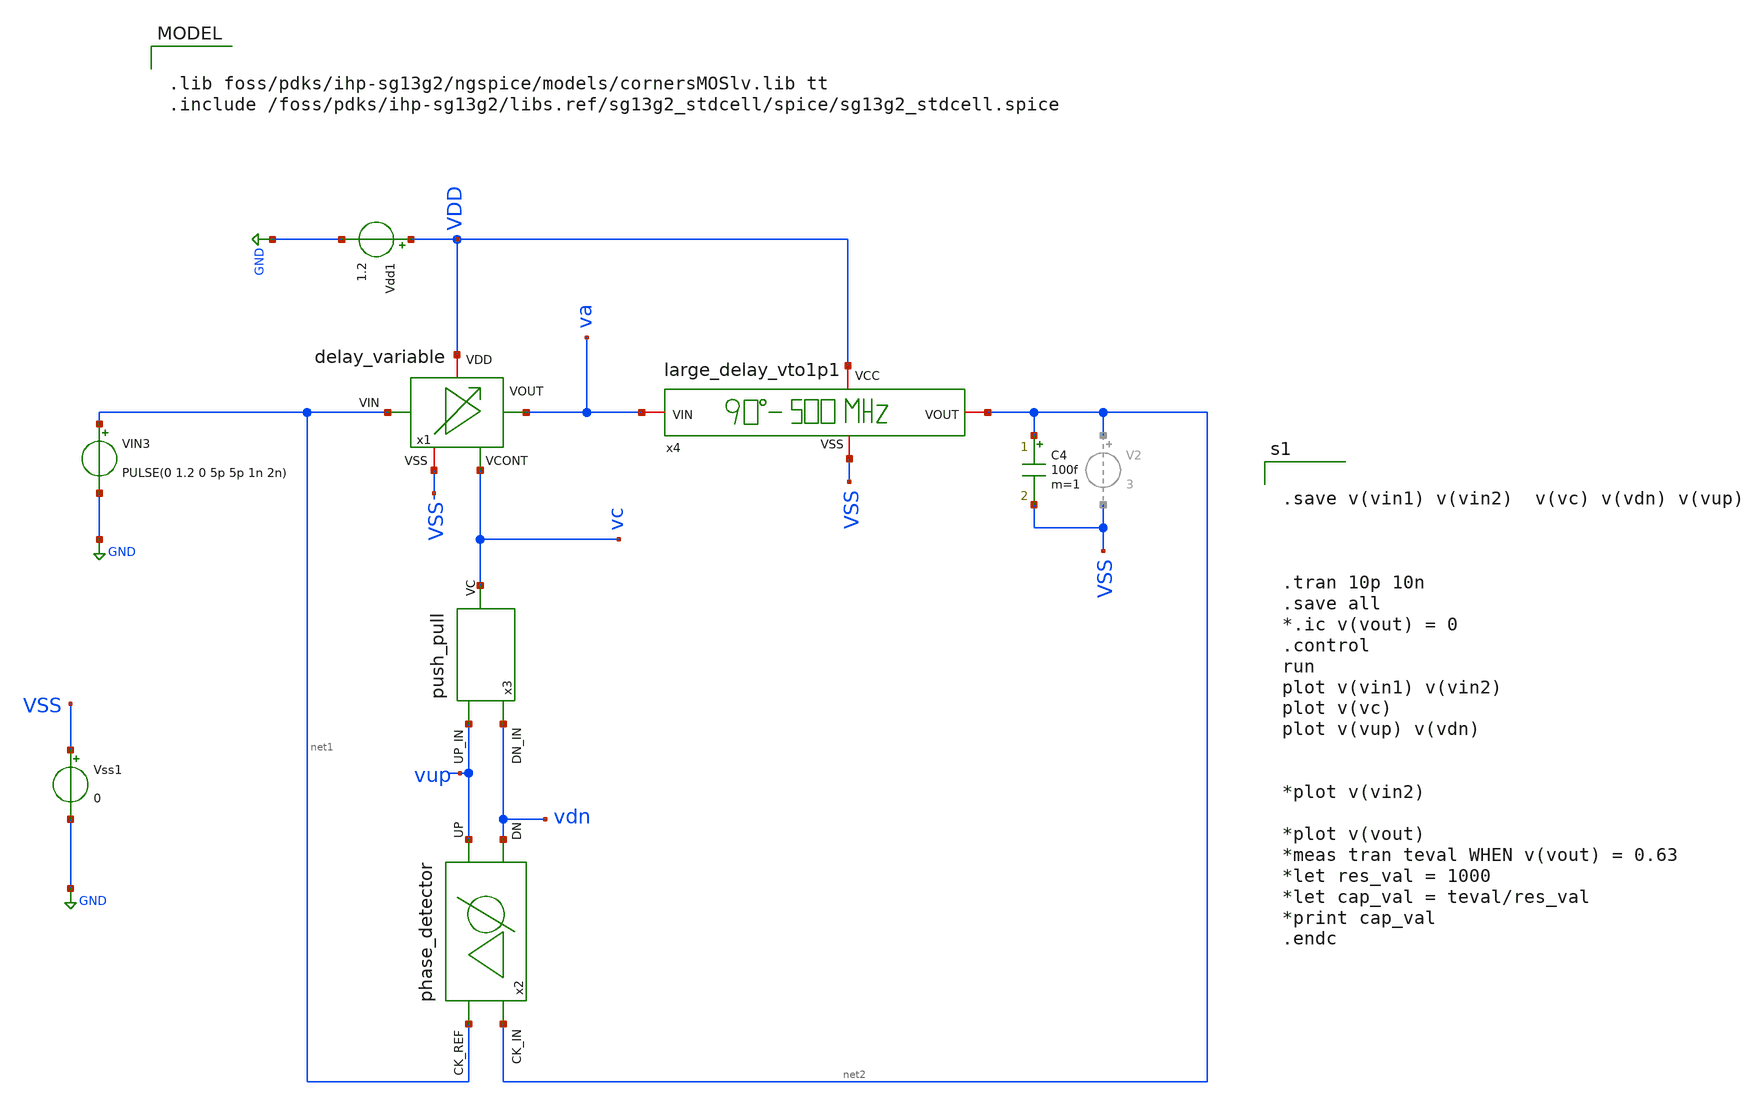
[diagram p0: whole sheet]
** sch_path: sch/DLL/DLL_tb.sch
**.subckt DLL_tb
Vdd1 VDD GND 1.2
C4 net2 VSS 100f m=1
VIN3 net1 GND PULSE(0 1.2 0 5p 5p 1n 2n)
Vss1 VSS GND 0
x4 VDD VSS va net2 large_delay_vto1p1
x1 VDD net1 va vc VSS delay_variable
x3 vup vc vdn push_pull
x2 net2 vup net1 vdn phase_detector
**** begin user architecture code


.save v(vin1) v(vin2)  v(vc) v(vdn) v(vup)



.tran 10p 10n
.save all
*.ic v(vout) = 0
.control
run
plot v(vin1) v(vin2)
plot v(vc)
plot v(vup) v(vdn)


*plot v(vin2)

*plot v(vout)
*meas tran teval WHEN v(vout) = 0.63
*let res_val = 1000
*let cap_val = teval/res_val
*print cap_val
.endc



.lib foss/pdks/ihp-sg13g2/ngspice/models/cornersMOSlv.lib tt
.include /foss/pdks/ihp-sg13g2/libs.ref/sg13g2_stdcell/spice/sg13g2_stdcell.spice

**** end user architecture code
**.ends
.GLOBAL GND
.end
